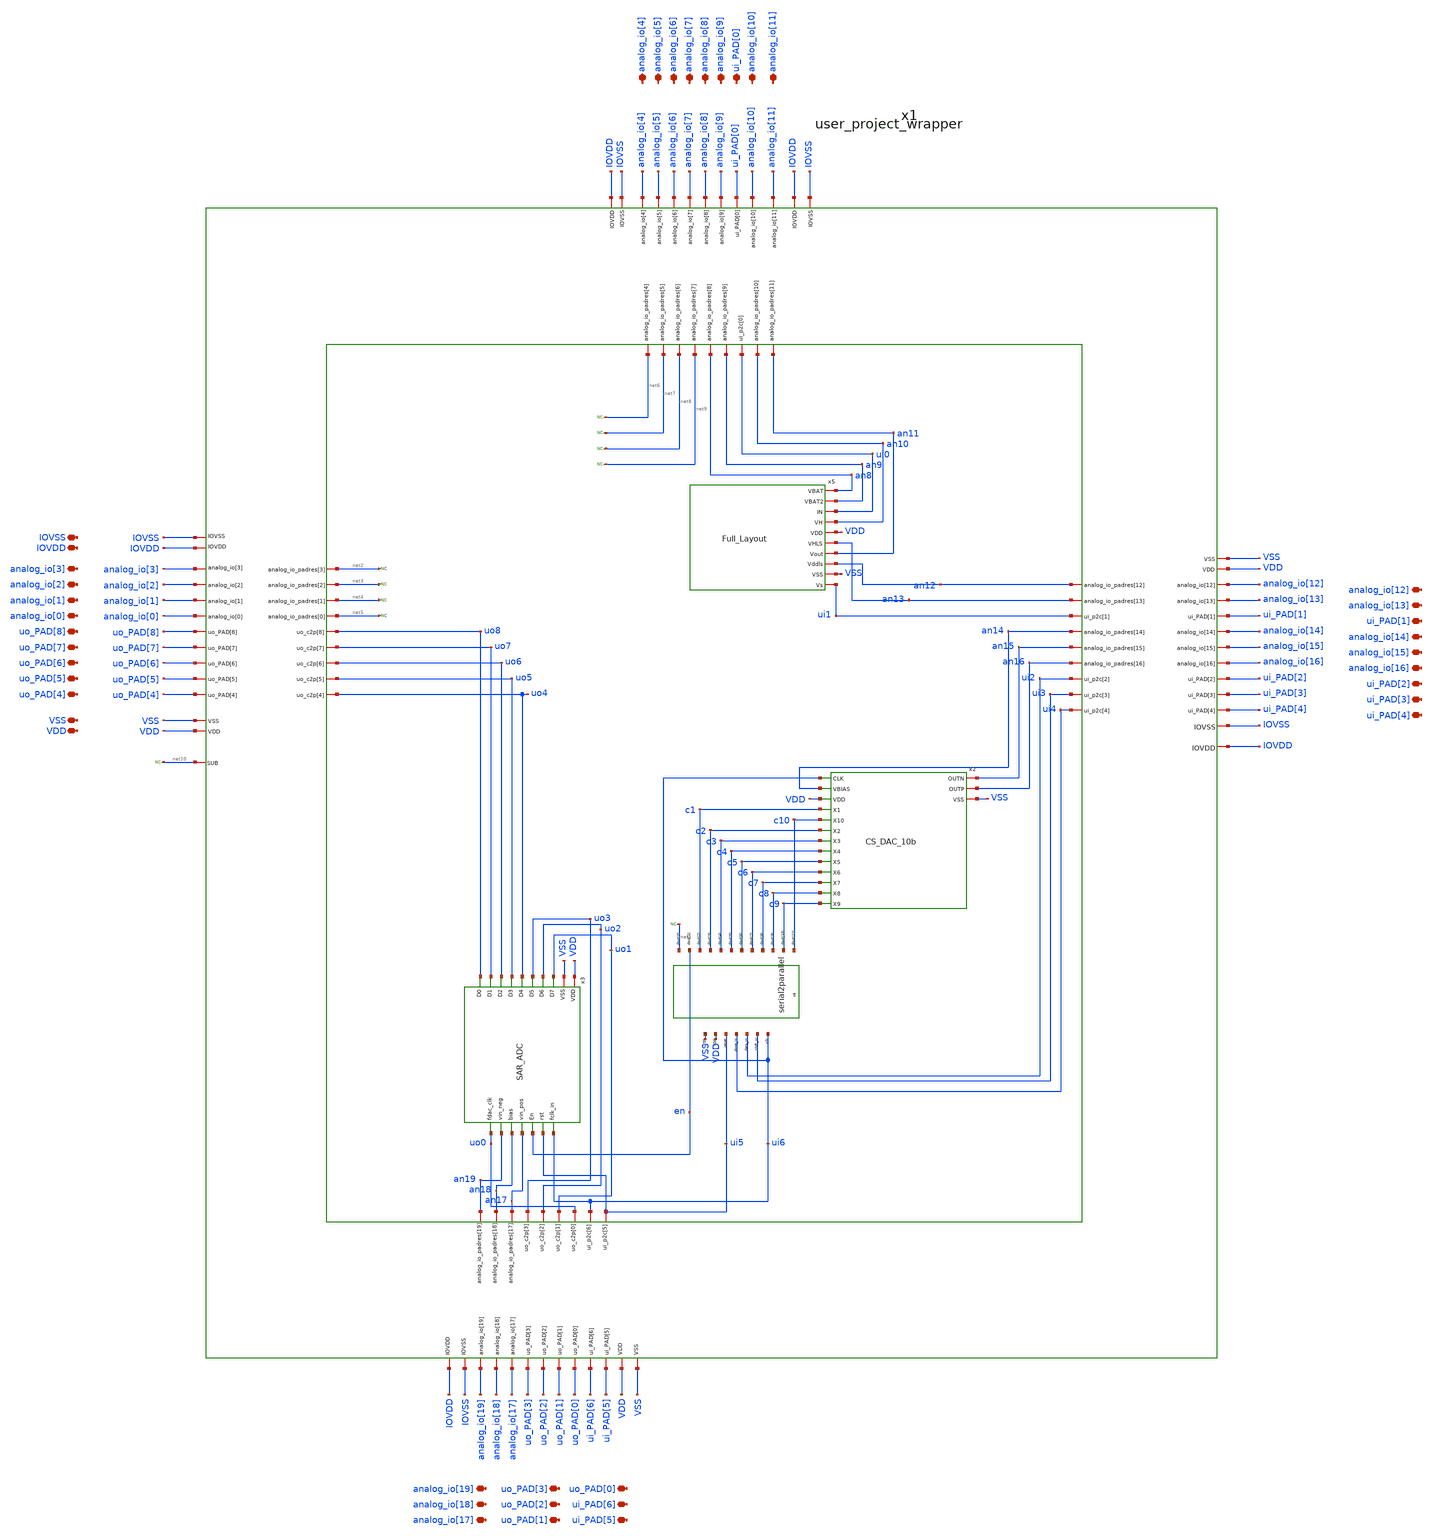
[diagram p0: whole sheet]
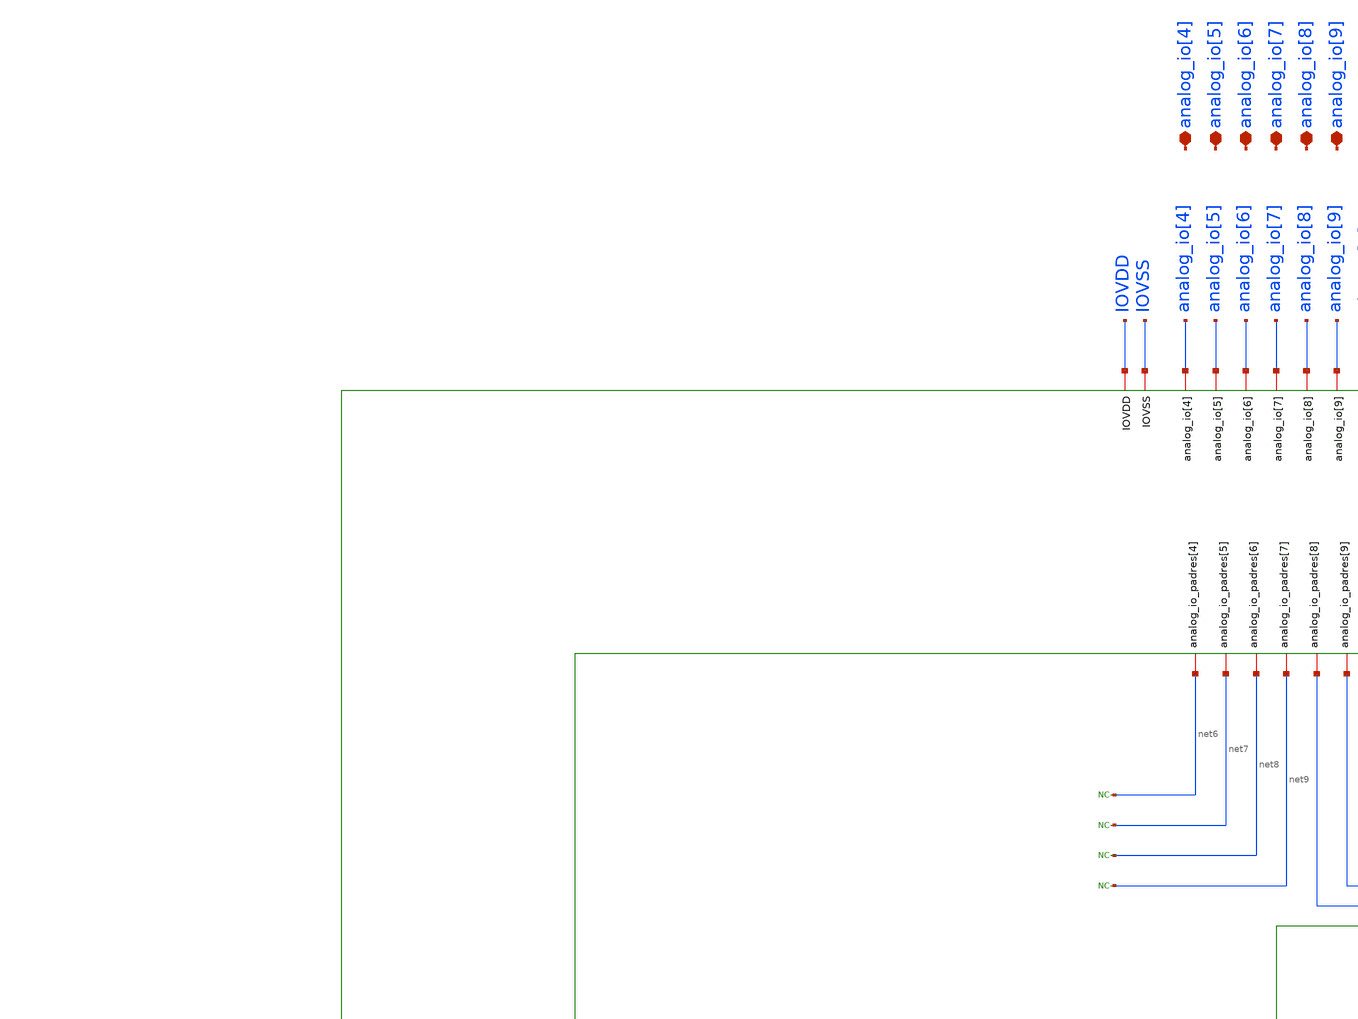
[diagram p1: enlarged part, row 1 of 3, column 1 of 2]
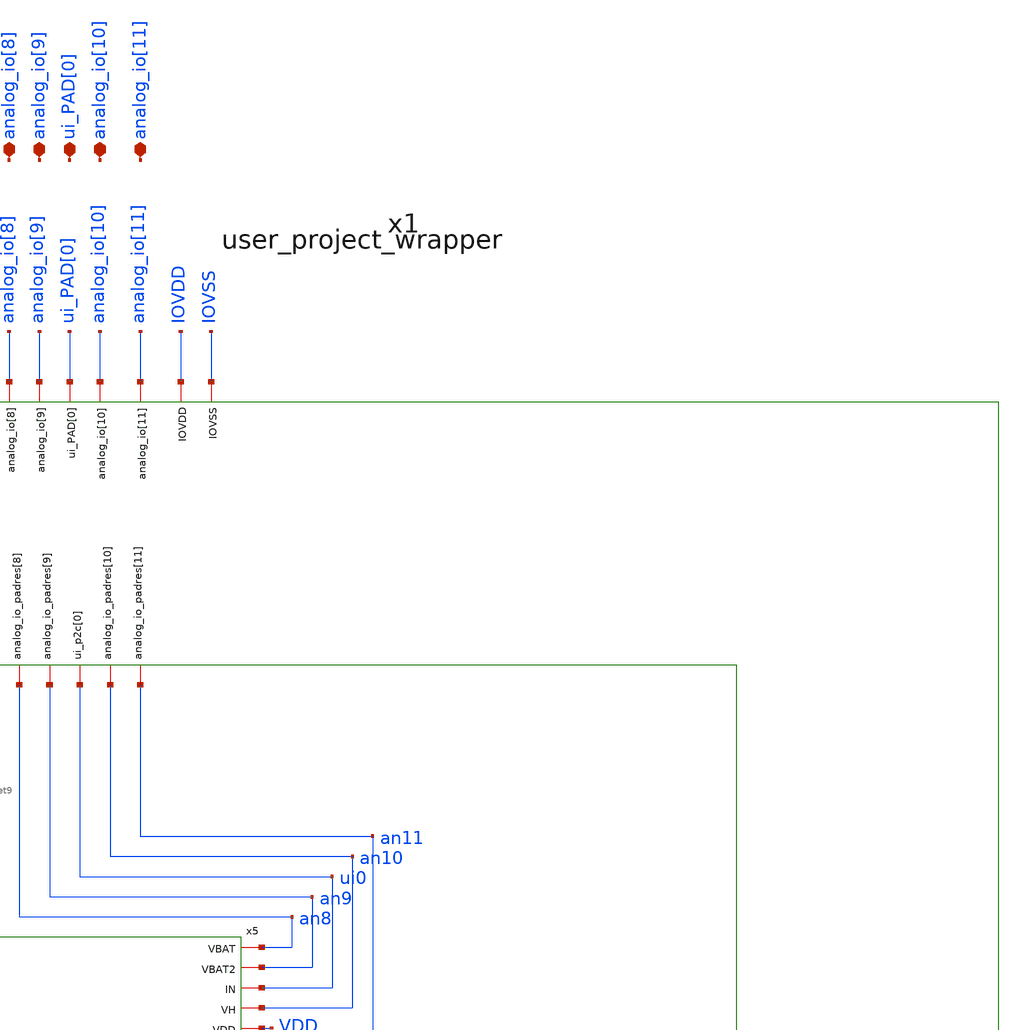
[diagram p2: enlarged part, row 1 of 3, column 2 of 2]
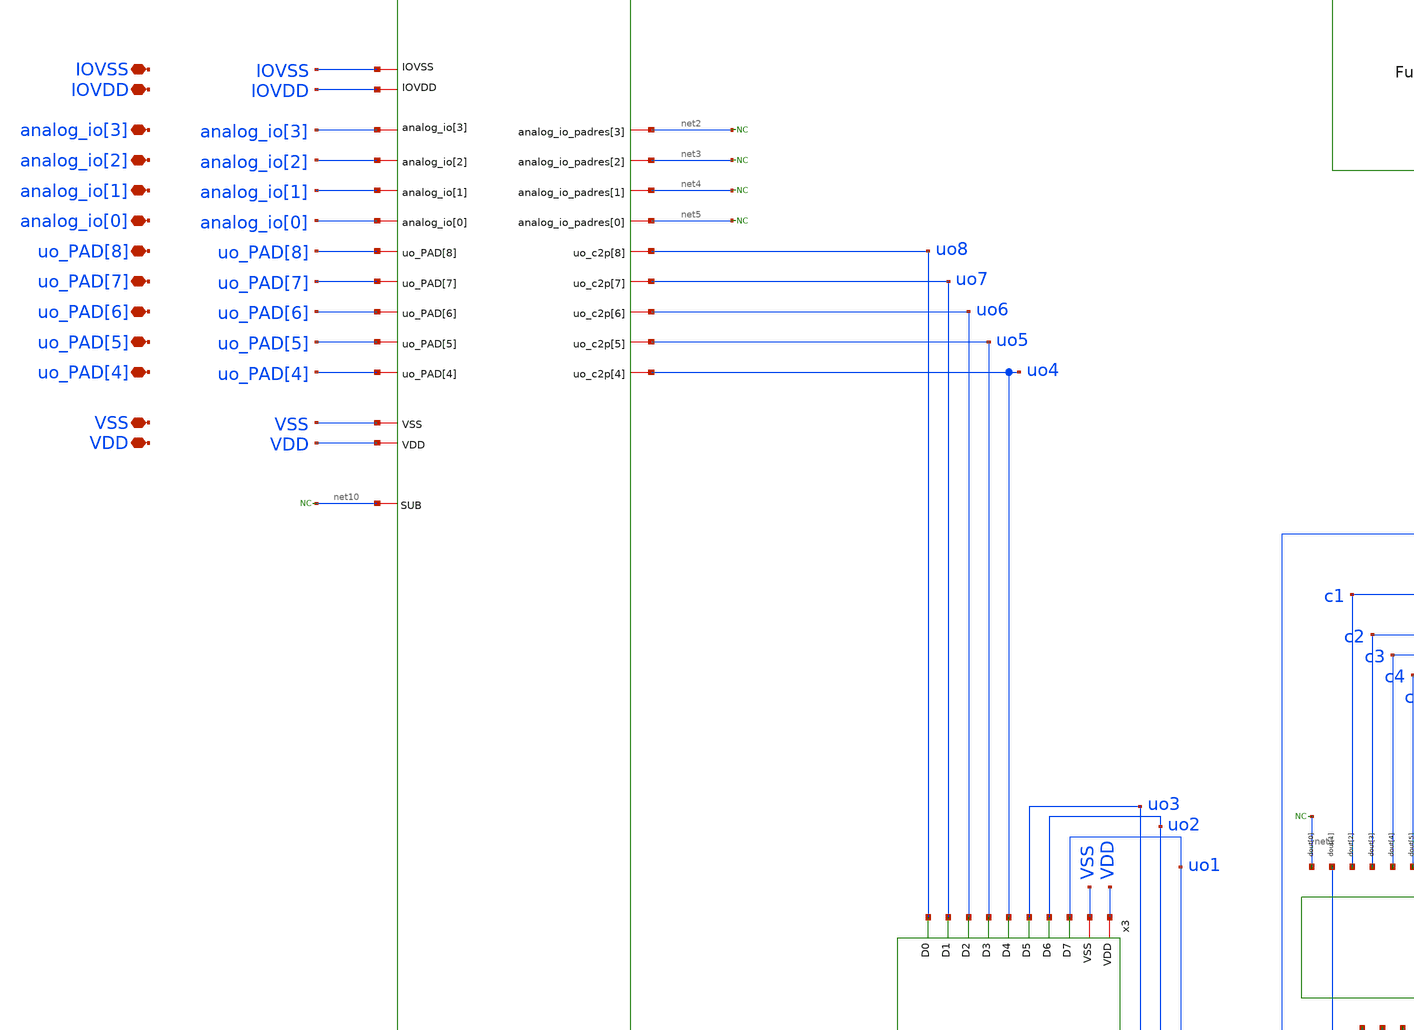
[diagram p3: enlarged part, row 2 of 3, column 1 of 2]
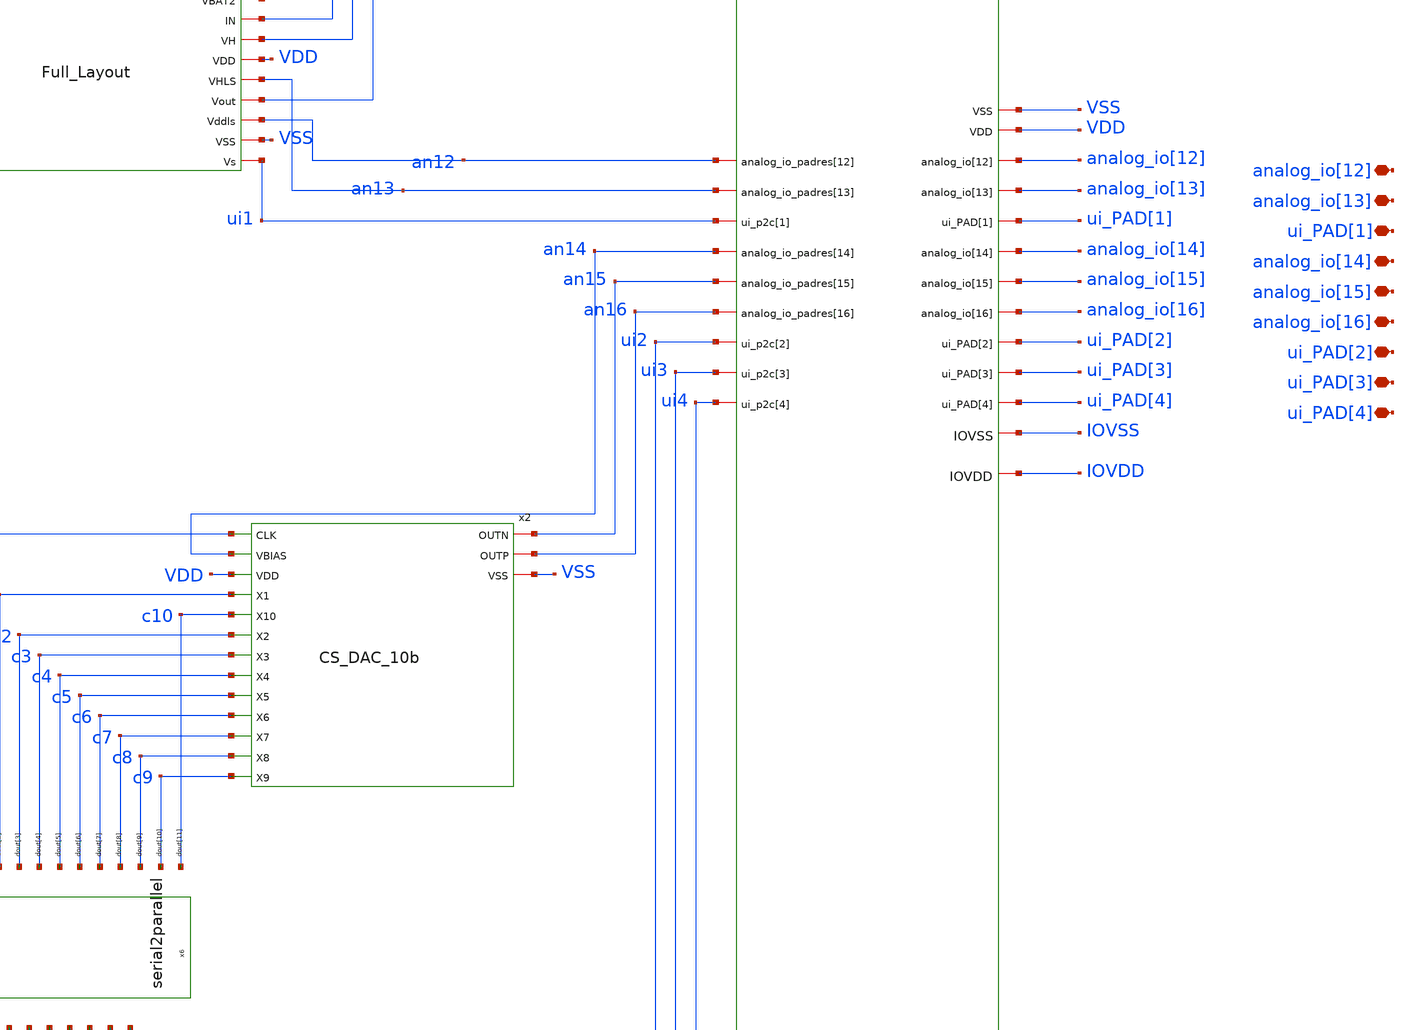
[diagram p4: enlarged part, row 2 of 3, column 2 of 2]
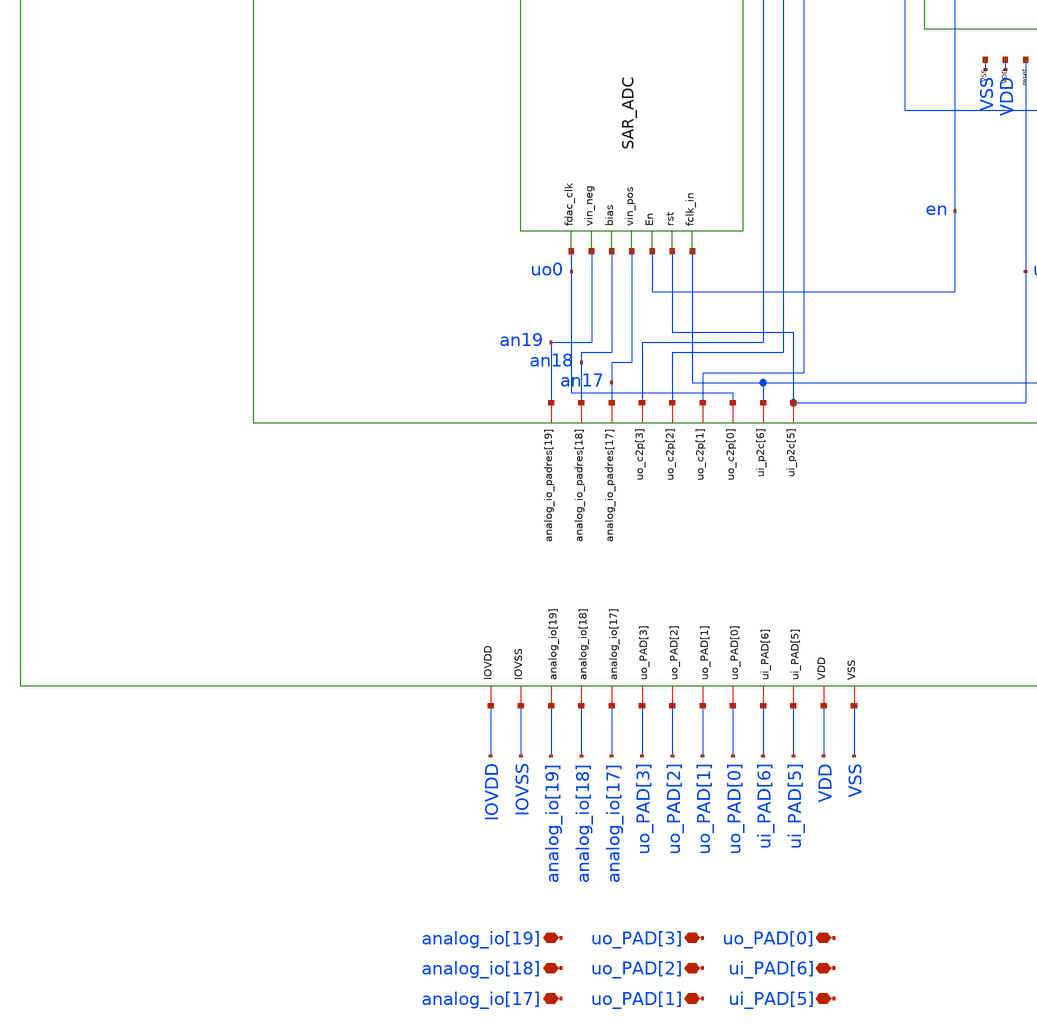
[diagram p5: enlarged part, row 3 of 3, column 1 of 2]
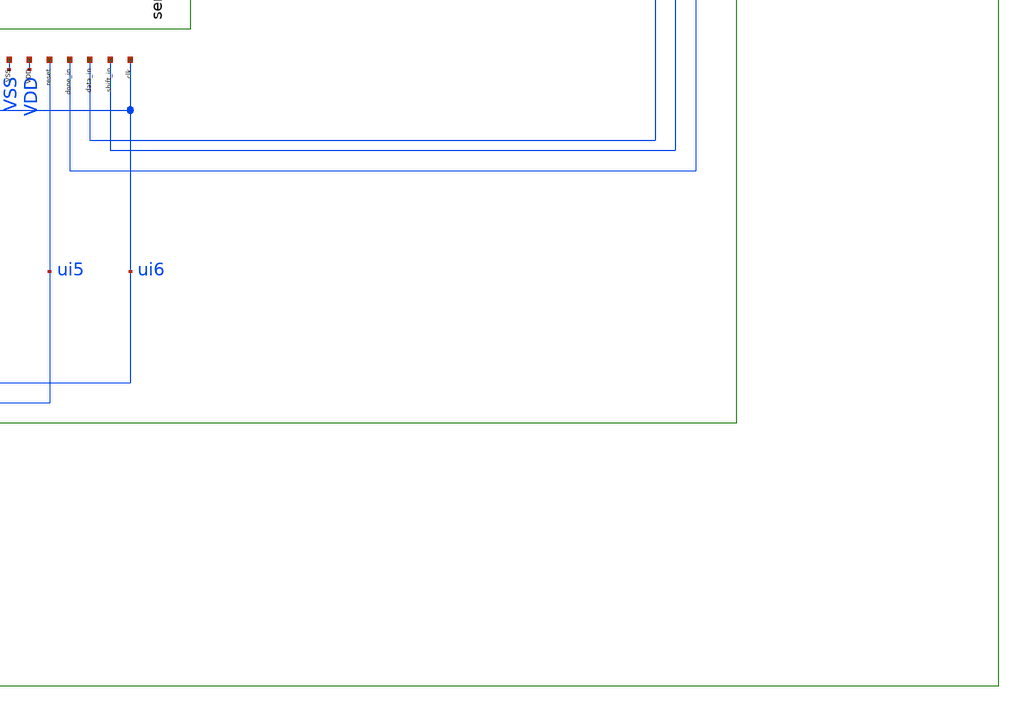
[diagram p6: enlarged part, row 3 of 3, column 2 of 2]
** sch_path: MSPHY6034-main/schematic/xschem/MSPHY6034.sch
**.subckt MSPHY6034 IOVSS IOVDD analog_io[3] analog_io[2] analog_io[1] analog_io[0] uo_PAD[8]
*+ uo_PAD[7] uo_PAD[6] uo_PAD[5] uo_PAD[4] VSS VDD analog_io[19] analog_io[18] analog_io[17] uo_PAD[3] uo_PAD[2]
*+ uo_PAD[1] uo_PAD[0] ui_PAD[6] ui_PAD[5] ui_PAD[4] ui_PAD[3] ui_PAD[2] analog_io[16] analog_io[15]
*+ analog_io[14] ui_PAD[1] analog_io[13] analog_io[12] analog_io[4] analog_io[5] analog_io[6] analog_io[7]
*+ analog_io[8] analog_io[9] ui_PAD[0] analog_io[10] analog_io[11]
*.iopin IOVSS
*.iopin IOVDD
*.iopin analog_io[3]
*.iopin analog_io[2]
*.iopin analog_io[1]
*.iopin analog_io[0]
*.iopin uo_PAD[8]
*.iopin uo_PAD[7]
*.iopin uo_PAD[6]
*.iopin uo_PAD[5]
*.iopin uo_PAD[4]
*.iopin VSS
*.iopin VDD
*.iopin analog_io[19]
*.iopin analog_io[18]
*.iopin analog_io[17]
*.iopin uo_PAD[3]
*.iopin uo_PAD[2]
*.iopin uo_PAD[1]
*.iopin uo_PAD[0]
*.iopin ui_PAD[6]
*.iopin ui_PAD[5]
*.iopin ui_PAD[4]
*.iopin ui_PAD[3]
*.iopin ui_PAD[2]
*.iopin analog_io[16]
*.iopin analog_io[15]
*.iopin analog_io[14]
*.iopin ui_PAD[1]
*.iopin analog_io[13]
*.iopin analog_io[12]
*.iopin analog_io[4]
*.iopin analog_io[5]
*.iopin analog_io[6]
*.iopin analog_io[7]
*.iopin analog_io[8]
*.iopin analog_io[9]
*.iopin ui_PAD[0]
*.iopin analog_io[10]
*.iopin analog_io[11]
x1 net10 analog_io[8] analog_io[6] analog_io[11] ui_PAD[0] analog_io[10] analog_io[7] analog_io[9]
+ analog_io[4] analog_io[5] net6 an11 net7 net8 ui0 an10 net9 an8 an9 an12 analog_io[3] analog_io[12] net2 an13
+ analog_io[2] analog_io[13] net3 ui1 analog_io[1] ui_PAD[1] net4 an14 analog_io[0] analog_io[14] net5 an15
+ uo_PAD[8] analog_io[15] an16 uo_PAD[7] analog_io[16] uo7 ui2 uo_PAD[6] ui_PAD[2] uo6 ui3 uo_PAD[5] ui_PAD[3]
+ uo5 ui4 uo_PAD[4] ui_PAD[4] uo4 ui5 ui6 uo0 uo1 uo2 uo3 an17 an18 an19 VSS VDD IOVDD IOVSS
+ analog_io[19] analog_io[18] analog_io[17] uo_PAD[3] uo_PAD[2] uo_PAD[1] uo_PAD[0] ui_PAD[6] ui_PAD[5] uo8
+ user_project_wrapper
x5 an8 an9 ui0 an10 VDD an13 an11 an12 VSS ui1 Full_Layout
x6 ui6 ui3 ui2 ui4 ui5 VDD VSS c10 c9 c8 c7 c6 c5 c4 c3 c2 c1 en net1 serial2parallel
* noconn #net1
* noconn #net6
* noconn #net7
* noconn #net8
* noconn #net9
* noconn #net2
* noconn #net3
* noconn #net4
* noconn #net5
* noconn #net10
x3 ui6 ui5 en VDD VSS uo0 an17 an18 an19 uo1 uo2 uo3 uo4 uo5 uo6 uo7 uo8 SAR_ADC
x2 ui6 an15 an16 an14 VDD VSS c1 c10 c2 c3 c4 c5 c6 c7 c8 c9 CS_DAC_10b
**.ends
.end
